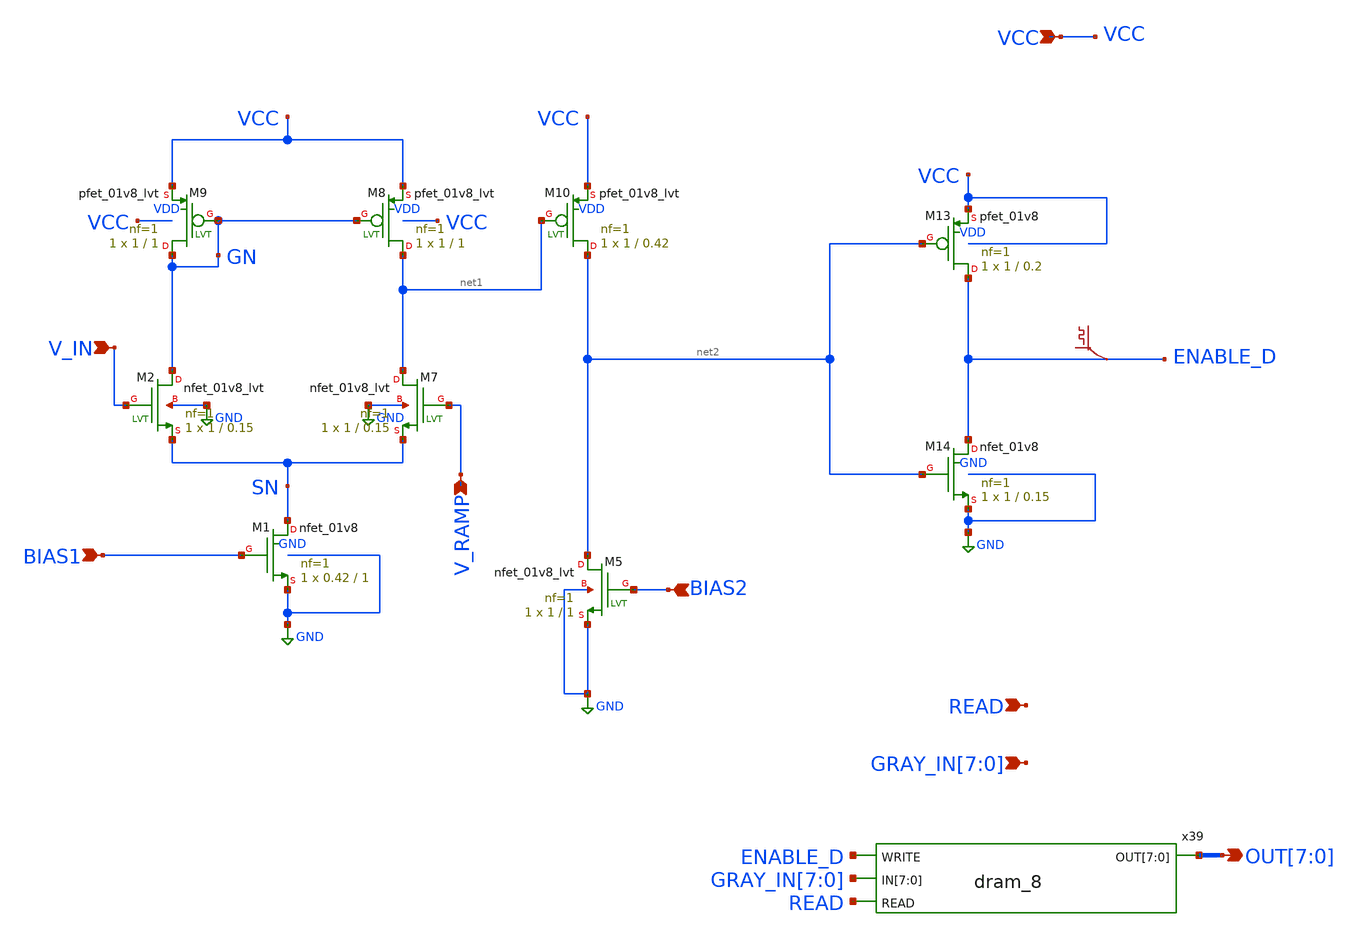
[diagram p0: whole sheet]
** sch_path: xschem/adc/8bit_adc.sch
**.subckt 8bit_adc VCC READ
*+ GRAY_IN[7],GRAY_IN[6],GRAY_IN[5],GRAY_IN[4],GRAY_IN[3],GRAY_IN[2],GRAY_IN[1],GRAY_IN[0] V_RAMP V_IN BIAS1 BIAS2 OUT[7],OUT[6],OUT[5],OUT[4],OUT[3],OUT[2],OUT[1],OUT[0]
*.ipin VCC
*.ipin READ
*.ipin GRAY_IN[7],GRAY_IN[6],GRAY_IN[5],GRAY_IN[4],GRAY_IN[3],GRAY_IN[2],GRAY_IN[1],GRAY_IN[0]
*.ipin V_RAMP
*.ipin V_IN
*.ipin BIAS1
*.ipin BIAS2
*.opin OUT[7],OUT[6],OUT[5],OUT[4],OUT[3],OUT[2],OUT[1],OUT[0]
XM2 GN V_IN SN GND sky130_fd_pr__nfet_01v8_lvt L=0.15 W=1 nf=1 ad='int((nf+1)/2) * W/nf * 0.29' as='int((nf+2)/2) * W/nf * 0.29'
+ pd='2*int((nf+1)/2) * (W/nf + 0.29)' ps='2*int((nf+2)/2) * (W/nf + 0.29)' nrd='0.29 / W' nrs='0.29 / W'
+ sa=0 sb=0 sd=0 mult=1 m=1
XM7 net1 V_RAMP SN GND sky130_fd_pr__nfet_01v8_lvt L=0.15 W=1 nf=1 ad='int((nf+1)/2) * W/nf * 0.29' as='int((nf+2)/2) * W/nf * 0.29'
+ pd='2*int((nf+1)/2) * (W/nf + 0.29)' ps='2*int((nf+2)/2) * (W/nf + 0.29)' nrd='0.29 / W' nrs='0.29 / W'
+ sa=0 sb=0 sd=0 mult=1 m=1
XM8 net1 GN VCC VDD sky130_fd_pr__pfet_01v8_lvt L=1 W=1 nf=1 ad='int((nf+1)/2) * W/nf * 0.29' as='int((nf+2)/2) * W/nf * 0.29'
+ pd='2*int((nf+1)/2) * (W/nf + 0.29)' ps='2*int((nf+2)/2) * (W/nf + 0.29)' nrd='0.29 / W' nrs='0.29 / W'
+ sa=0 sb=0 sd=0 mult=1 m=1
XM9 GN GN VCC VDD sky130_fd_pr__pfet_01v8_lvt L=1 W=1 nf=1 ad='int((nf+1)/2) * W/nf * 0.29' as='int((nf+2)/2) * W/nf * 0.29'
+ pd='2*int((nf+1)/2) * (W/nf + 0.29)' ps='2*int((nf+2)/2) * (W/nf + 0.29)' nrd='0.29 / W' nrs='0.29 / W'
+ sa=0 sb=0 sd=0 mult=1 m=1
XM10 net2 net1 VCC VDD sky130_fd_pr__pfet_01v8_lvt L=0.42 W=1 nf=1 ad='int((nf+1)/2) * W/nf * 0.29' as='int((nf+2)/2) * W/nf * 0.29'
+ pd='2*int((nf+1)/2) * (W/nf + 0.29)' ps='2*int((nf+2)/2) * (W/nf + 0.29)' nrd='0.29 / W' nrs='0.29 / W'
+ sa=0 sb=0 sd=0 mult=1 m=1
XM13 ENABLE_D net2 VCC VDD sky130_fd_pr__pfet_01v8 L=0.2 W=1 nf=1 ad='int((nf+1)/2) * W/nf * 0.29' as='int((nf+2)/2) * W/nf * 0.29'
+ pd='2*int((nf+1)/2) * (W/nf + 0.29)' ps='2*int((nf+2)/2) * (W/nf + 0.29)' nrd='0.29 / W' nrs='0.29 / W'
+ sa=0 sb=0 sd=0 mult=1 m=1
XM14 ENABLE_D net2 GND GND sky130_fd_pr__nfet_01v8 L=0.15 W=1 nf=1 ad='int((nf+1)/2) * W/nf * 0.29' as='int((nf+2)/2) * W/nf * 0.29'
+ pd='2*int((nf+1)/2) * (W/nf + 0.29)' ps='2*int((nf+2)/2) * (W/nf + 0.29)' nrd='0.29 / W' nrs='0.29 / W'
+ sa=0 sb=0 sd=0 mult=1 m=1
.save v(enable_d)
XM1 SN BIAS1 GND GND sky130_fd_pr__nfet_01v8 L=1 W=0.42 nf=1 ad='int((nf+1)/2) * W/nf * 0.29' as='int((nf+2)/2) * W/nf * 0.29'
+ pd='2*int((nf+1)/2) * (W/nf + 0.29)' ps='2*int((nf+2)/2) * (W/nf + 0.29)' nrd='0.29 / W' nrs='0.29 / W'
+ sa=0 sb=0 sd=0 mult=1 m=1
XM5 net2 BIAS2 GND GND sky130_fd_pr__nfet_01v8_lvt L=1 W=1 nf=1 ad='int((nf+1)/2) * W/nf * 0.29' as='int((nf+2)/2) * W/nf * 0.29'
+ pd='2*int((nf+1)/2) * (W/nf + 0.29)' ps='2*int((nf+2)/2) * (W/nf + 0.29)' nrd='0.29 / W' nrs='0.29 / W'
+ sa=0 sb=0 sd=0 mult=1 m=1
x39 OUT[7] OUT[6] OUT[5] OUT[4] OUT[3] OUT[2] OUT[1] OUT[0] ENABLE_D GRAY_IN[7] GRAY_IN[6]
+ GRAY_IN[5] GRAY_IN[4] GRAY_IN[3] GRAY_IN[2] GRAY_IN[1] GRAY_IN[0] READ dram_8
**.ends

* expanding   symbol:  digital_prims/dram_8.sym # of pins=4
** sym_path: xschem/digital_prims/dram_8.sym
** sch_path: xschem/digital_prims/dram_8.sch
.subckt dram_8 OUT[7] OUT[6] OUT[5] OUT[4] OUT[3] OUT[2] OUT[1] OUT[0] WRITE IN[7] IN[6] IN[5] IN[4]
+ IN[3] IN[2] IN[1] IN[0] READ
*.opin OUT[7],OUT[6],OUT[5],OUT[4],OUT[3],OUT[2],OUT[1],OUT[0]
*.ipin WRITE
*.ipin IN[7],IN[6],IN[5],IN[4],IN[3],IN[2],IN[1],IN[0]
*.ipin READ
x5 WRITE OUT[7] net8 IN[7] READ net8 dram
x6 WRITE OUT[6] net7 IN[6] READ net7 dram
x7 WRITE OUT[5] net6 IN[5] READ net6 dram
x25 WRITE OUT[4] net5 IN[4] READ net5 dram
x26 WRITE OUT[3] net4 IN[3] READ net4 dram
x27 WRITE OUT[2] net3 IN[2] READ net3 dram
x33 WRITE OUT[1] net2 IN[0] READ net2 dram
x34 WRITE OUT[0] net1 IN[1] READ net1 dram
.ends


* expanding   symbol:  digital_prims/dram.sym # of pins=6
** sym_path: xschem/digital_prims/dram.sym
** sch_path: xschem/digital_prims/dram.sch
.subckt dram WWL RBL storage WBL RWL GND
*.opin RBL
*.ipin RWL
*.ipin WBL
*.ipin WWL
*.opin storage
*.ipin GND
XM3 RWL storage RBL GND sky130_fd_pr__nfet_01v8 L=0.15 W=1 nf=1 ad='int((nf+1)/2) * W/nf * 0.29' as='int((nf+2)/2) * W/nf * 0.29'
+ pd='2*int((nf+1)/2) * (W/nf + 0.29)' ps='2*int((nf+2)/2) * (W/nf + 0.29)' nrd='0.29 / W' nrs='0.29 / W'
+ sa=0 sb=0 sd=0 mult=1 m=1
XM1 WBL WWL storage GND sky130_fd_pr__nfet_01v8 L=0.15 W=1 nf=1 ad='int((nf+1)/2) * W/nf * 0.29' as='int((nf+2)/2) * W/nf * 0.29'
+ pd='2*int((nf+1)/2) * (W/nf + 0.29)' ps='2*int((nf+2)/2) * (W/nf + 0.29)' nrd='0.29 / W' nrs='0.29 / W'
+ sa=0 sb=0 sd=0 mult=1 m=1
.ends

.GLOBAL GND
.end
